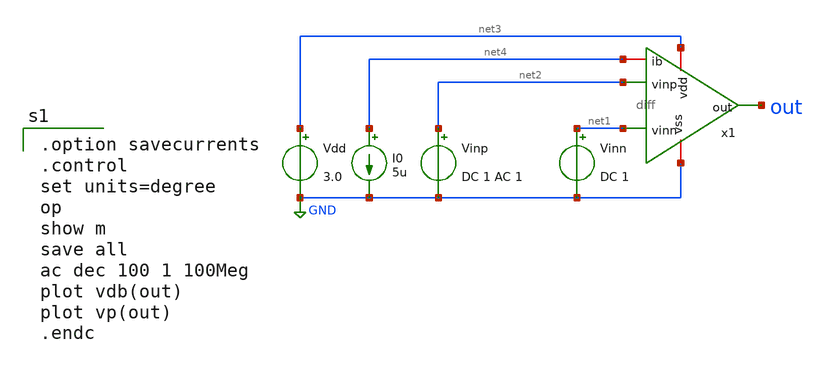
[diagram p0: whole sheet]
** sch_path: member_project/DCDC/xschem/diff_ac.sch
**.subckt diff_ac
Vinn net1 GND DC 1
Vinp net2 GND DC 1 AC 1
Vdd net3 GND 3.0
I0 net4 GND 5u
x1 net3 net4 net1 out net2 GND diff
**** begin user architecture code
 .include $::LIB/ip62_models

.option savecurrents
.control
set units=degree
op
show m
save all
ac dec 100 1 100Meg
plot vdb(out)
plot vp(out)
.endc

**** end user architecture code
**.ends
.GLOBAL GND
.end
